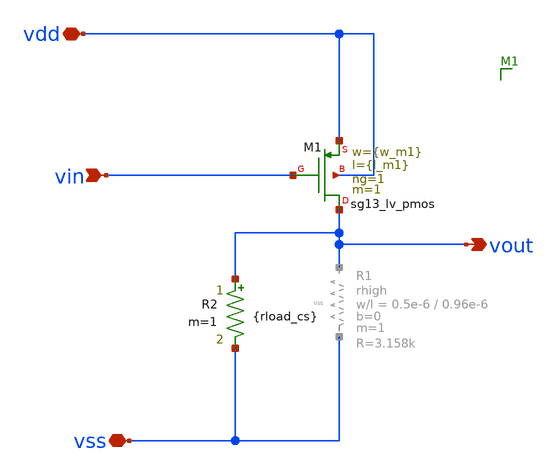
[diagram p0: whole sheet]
** sch_path: macros/amp_cs/schematic/xschem/amp_cs.sch
**.subckt amp_cs vin vout vdd vss
*.ipin vin
*.opin vout
*.iopin vdd
*.iopin vss
XM1 vout vin vdd vdd sg13_lv_pmos w={w_m1} l={l_m1} ng=1 m=1 mm_ok=1
R2 vout vss {rload_cs} m=1
**.ends
.end
